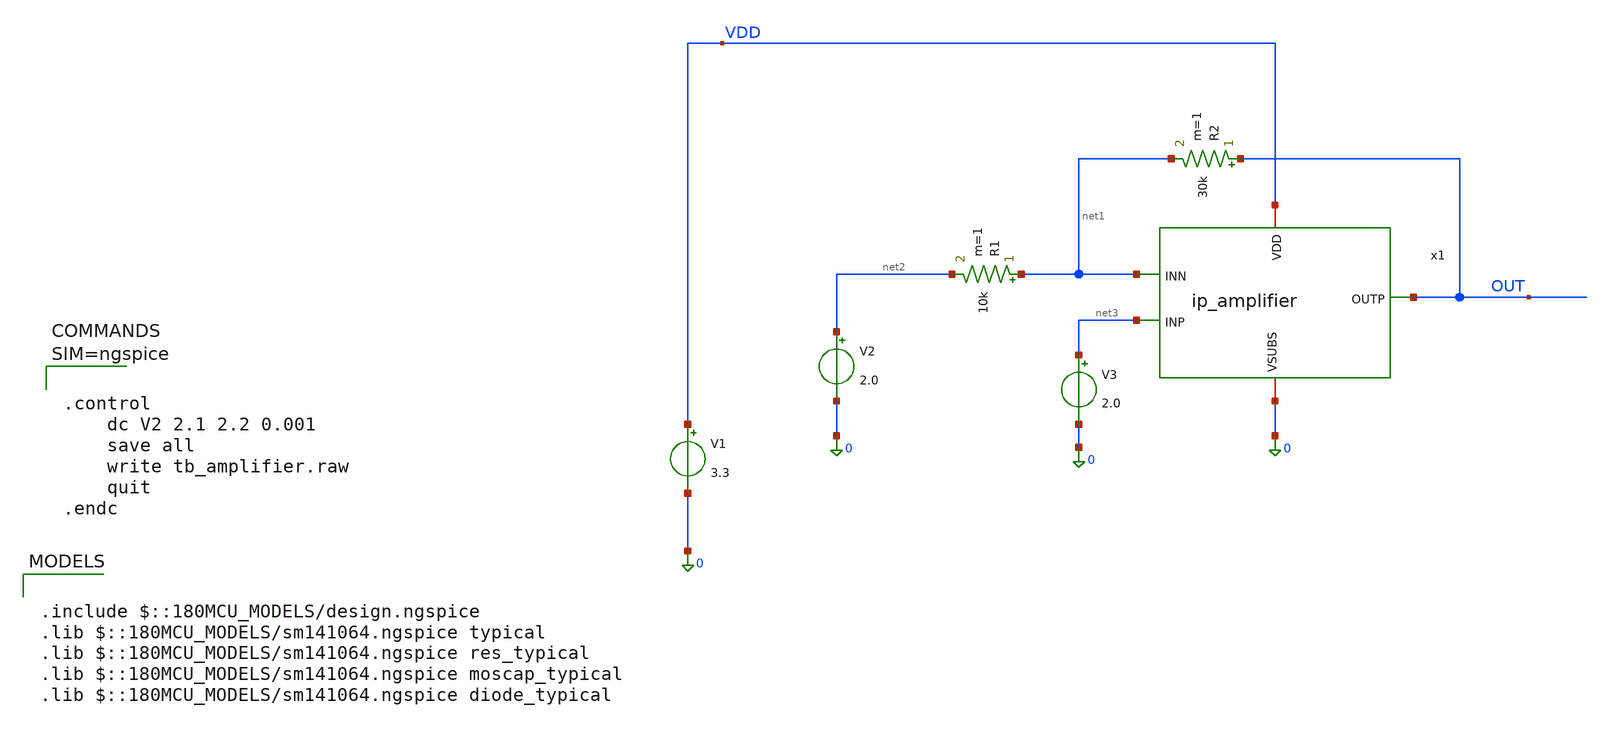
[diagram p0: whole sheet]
** sch_path: xschem/tb_amplifier.sch
**.subckt tb_amplifier
V1 VDD 0 3.3
x1 VDD OUT net3 net1 0 ip_amplifier
V2 net2 0 2.0
R1 net1 net2 10k m=1
R2 OUT net1 30k m=1
V3 net3 0 2.0
**** begin user architecture code

.include $::180MCU_MODELS/design.ngspice
.lib $::180MCU_MODELS/sm141064.ngspice typical
.lib $::180MCU_MODELS/sm141064.ngspice res_typical
.lib $::180MCU_MODELS/sm141064.ngspice moscap_typical
.lib $::180MCU_MODELS/sm141064.ngspice diode_typical




.control
	dc V2 2.1 2.2 0.001
	save all
	write tb_amplifier.raw
	quit
.endc



**** end user architecture code
**.ends

* expanding   symbol:  ip_amplifier.sym # of pins=5
** sym_path: xschem/ip_amplifier.sym
** sch_path: xschem/ip_amplifier.sch
.subckt ip_amplifier VDD OUTP INP INN VSUBS
*.iopin VDD
*.iopin VSUBS
*.ipin INP
*.ipin INN
*.opin OUTP
XM1 COM_P COM_P VDD VDD pfet_03v3 L=1.0u W=1.0u nf=1 ad='int((nf+1)/2) * W/nf * 0.18u' as='int((nf+2)/2) * W/nf * 0.18u'
+ pd='2*int((nf+1)/2) * (W/nf + 0.18u)' ps='2*int((nf+2)/2) * (W/nf + 0.18u)' nrd='0.18u / W' nrs='0.18u / W'
+ sa=0 sb=0 sd=0 m=1 par=1
XM2 net3 net1 net2 VSUBS nfet_03v3 L=0.5u W=5.0u nf=1 ad='int((nf+1)/2) * W/nf * 0.18u' as='int((nf+2)/2) * W/nf * 0.18u'
+ pd='2*int((nf+1)/2) * (W/nf + 0.18u)' ps='2*int((nf+2)/2) * (W/nf + 0.18u)' nrd='0.18u / W' nrs='0.18u / W'
+ sa=0 sb=0 sd=0 m=1 par=1
XM3 net2 net1 VSUBS VSUBS nfet_03v3 L=1.0u W=1.0u nf=1 ad='int((nf+1)/2) * W/nf * 0.18u' as='int((nf+2)/2) * W/nf * 0.18u'
+ pd='2*int((nf+1)/2) * (W/nf + 0.18u)' ps='2*int((nf+2)/2) * (W/nf + 0.18u)' nrd='0.18u / W' nrs='0.18u / W'
+ sa=0 sb=0 sd=0 m=1 par=1
XM4 net1 net1 VSUBS VSUBS nfet_03v3 L=1.0u W=1.0u nf=1 ad='int((nf+1)/2) * W/nf * 0.18u' as='int((nf+2)/2) * W/nf * 0.18u'
+ pd='2*int((nf+1)/2) * (W/nf + 0.18u)' ps='2*int((nf+2)/2) * (W/nf + 0.18u)' nrd='0.18u / W' nrs='0.18u / W'
+ sa=0 sb=0 sd=0 m=1 par=1
XM5 net4 COM_P VDD VDD pfet_03v3 L=2.0u W=1.0u nf=1 ad='int((nf+1)/2) * W/nf * 0.18u' as='int((nf+2)/2) * W/nf * 0.18u'
+ pd='2*int((nf+1)/2) * (W/nf + 0.18u)' ps='2*int((nf+2)/2) * (W/nf + 0.18u)' nrd='0.18u / W' nrs='0.18u / W'
+ sa=0 sb=0 sd=0 m=1 par=1
XM6 net1 COM_P net4 VDD pfet_03v3 L=0.5u W=5.0u nf=1 ad='int((nf+1)/2) * W/nf * 0.18u' as='int((nf+2)/2) * W/nf * 0.18u'
+ pd='2*int((nf+1)/2) * (W/nf + 0.18u)' ps='2*int((nf+2)/2) * (W/nf + 0.18u)' nrd='0.18u / W' nrs='0.18u / W'
+ sa=0 sb=0 sd=0 m=1 par=1
XM7 DIFF_L COM_P VDD VDD pfet_03v3 L=2.0u W=1.0u nf=1 ad='int((nf+1)/2) * W/nf * 0.18u' as='int((nf+2)/2) * W/nf * 0.18u'
+ pd='2*int((nf+1)/2) * (W/nf + 0.18u)' ps='2*int((nf+2)/2) * (W/nf + 0.18u)' nrd='0.18u / W' nrs='0.18u / W'
+ sa=0 sb=0 sd=0 m=1 par=1
XM9 DIFF_R COM_P VDD VDD pfet_03v3 L=2.0u W=1.0u nf=1 ad='int((nf+1)/2) * W/nf * 0.18u' as='int((nf+2)/2) * W/nf * 0.18u'
+ pd='2*int((nf+1)/2) * (W/nf + 0.18u)' ps='2*int((nf+2)/2) * (W/nf + 0.18u)' nrd='0.18u / W' nrs='0.18u / W'
+ sa=0 sb=0 sd=0 m=1 par=1
XM11 DIFF_L INP net3 VSUBS nfet_03v3 L=1.5u W=5.0u nf=1 ad='int((nf+1)/2) * W/nf * 0.18u' as='int((nf+2)/2) * W/nf * 0.18u'
+ pd='2*int((nf+1)/2) * (W/nf + 0.18u)' ps='2*int((nf+2)/2) * (W/nf + 0.18u)' nrd='0.18u / W' nrs='0.18u / W'
+ sa=0 sb=0 sd=0 m=1 par=1
XM12 DIFF_R INN net3 VSUBS nfet_03v3 L=1.5u W=5.0u nf=1 ad='int((nf+1)/2) * W/nf * 0.18u' as='int((nf+2)/2) * W/nf * 0.18u'
+ pd='2*int((nf+1)/2) * (W/nf + 0.18u)' ps='2*int((nf+2)/2) * (W/nf + 0.18u)' nrd='0.18u / W' nrs='0.18u / W'
+ sa=0 sb=0 sd=0 m=1 par=1
XM8 net5 COM_P DIFF_L VDD pfet_03v3 L=0.5u W=5.0u nf=1 ad='int((nf+1)/2) * W/nf * 0.18u' as='int((nf+2)/2) * W/nf * 0.18u'
+ pd='2*int((nf+1)/2) * (W/nf + 0.18u)' ps='2*int((nf+2)/2) * (W/nf + 0.18u)' nrd='0.18u / W' nrs='0.18u / W'
+ sa=0 sb=0 sd=0 m=1 par=1
XM10 net6 COM_P DIFF_R VDD pfet_03v3 L=0.5u W=5.0u nf=1 ad='int((nf+1)/2) * W/nf * 0.18u' as='int((nf+2)/2) * W/nf * 0.18u'
+ pd='2*int((nf+1)/2) * (W/nf + 0.18u)' ps='2*int((nf+2)/2) * (W/nf + 0.18u)' nrd='0.18u / W' nrs='0.18u / W'
+ sa=0 sb=0 sd=0 m=1 par=1
XM13 net6 net5 VSUBS VSUBS nfet_03v3 L=1.0u W=1.0u nf=1 ad='int((nf+1)/2) * W/nf * 0.18u' as='int((nf+2)/2) * W/nf * 0.18u'
+ pd='2*int((nf+1)/2) * (W/nf + 0.18u)' ps='2*int((nf+2)/2) * (W/nf + 0.18u)' nrd='0.18u / W' nrs='0.18u / W'
+ sa=0 sb=0 sd=0 m=1 par=1
XM14 net5 net5 VSUBS VSUBS nfet_03v3 L=1.0u W=1.0u nf=1 ad='int((nf+1)/2) * W/nf * 0.18u' as='int((nf+2)/2) * W/nf * 0.18u'
+ pd='2*int((nf+1)/2) * (W/nf + 0.18u)' ps='2*int((nf+2)/2) * (W/nf + 0.18u)' nrd='0.18u / W' nrs='0.18u / W'
+ sa=0 sb=0 sd=0 m=1 par=1
XM15 OUTP COM_P VDD VDD pfet_03v3 L=1.0u W=10u nf=1 ad='int((nf+1)/2) * W/nf * 0.18u' as='int((nf+2)/2) * W/nf * 0.18u'
+ pd='2*int((nf+1)/2) * (W/nf + 0.18u)' ps='2*int((nf+2)/2) * (W/nf + 0.18u)' nrd='0.18u / W' nrs='0.18u / W'
+ sa=0 sb=0 sd=0 m=1 par=1
XM16 OUTP net6 VSUBS VSUBS nfet_03v3 L=1.0u W=10.0u nf=1 ad='int((nf+1)/2) * W/nf * 0.18u' as='int((nf+2)/2) * W/nf * 0.18u'
+ pd='2*int((nf+1)/2) * (W/nf + 0.18u)' ps='2*int((nf+2)/2) * (W/nf + 0.18u)' nrd='0.18u / W' nrs='0.18u / W'
+ sa=0 sb=0 sd=0 m=1 par=1
R1 COM_P VSUBS 36k m=1
.ends

.end
